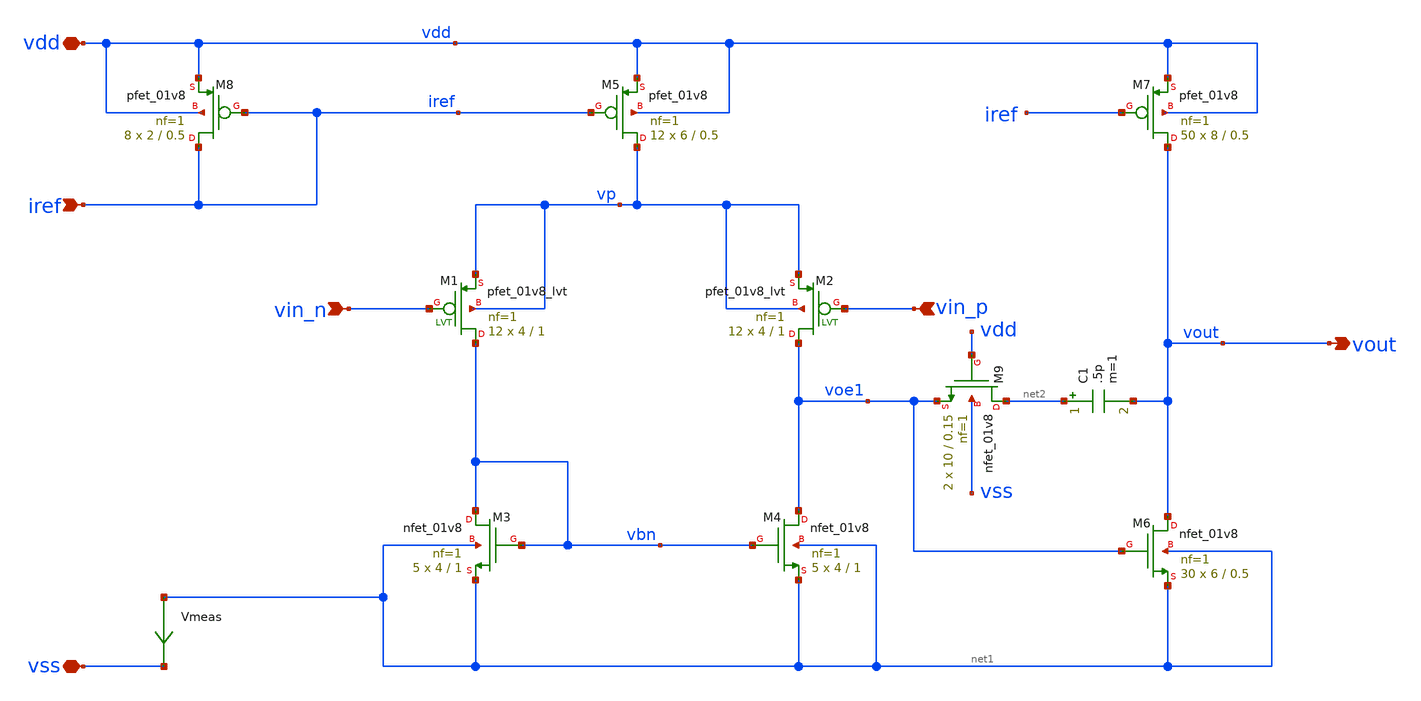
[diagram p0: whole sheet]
** sch_path: opamp/opamp.sch
**.subckt opamp vdd vss vin_n vin_p iref vout
*.iopin vdd
*.iopin vss
*.ipin vin_n
*.ipin vin_p
*.ipin iref
*.opin vout
XM3 vbn vbn net1 net1 sky130_fd_pr__nfet_01v8 L=1 W=4 nf=1 ad='W * 0.29' as='W * 0.29' pd='2 * (W + 0.29)'
+ ps='2 * (W + 0.29)' nrd='0.29 / W' nrs='0.29 / W' sa=0 sb=0 sd=0 mult=5 m=5
XM4 voe1 vbn net1 net1 sky130_fd_pr__nfet_01v8 L=1 W=4 nf=1 ad='W * 0.29' as='W * 0.29' pd='2 * (W + 0.29)'
+ ps='2 * (W + 0.29)' nrd='0.29 / W' nrs='0.29 / W' sa=0 sb=0 sd=0 mult=5 m=5
XM5 vp iref vdd vdd sky130_fd_pr__pfet_01v8 L=0.5 W=6 nf=1 ad='W * 0.29' as='W * 0.29' pd='2 * (W + 0.29)'
+ ps='2 * (W + 0.29)' nrd='0.29 / W' nrs='0.29 / W' sa=0 sb=0 sd=0 mult=12 m=12
XM7 vout iref vdd vdd sky130_fd_pr__pfet_01v8 L=0.5 W=8 nf=1 ad='W * 0.29' as='W * 0.29' pd='2 * (W + 0.29)'
+ ps='2 * (W + 0.29)' nrd='0.29 / W' nrs='0.29 / W' sa=0 sb=0 sd=0 mult=50 m=50
XM8 iref iref vdd vdd sky130_fd_pr__pfet_01v8 L=0.5 W=2 nf=1 ad='W * 0.29' as='W * 0.29' pd='2 * (W + 0.29)'
+ ps='2 * (W + 0.29)' nrd='0.29 / W' nrs='0.29 / W' sa=0 sb=0 sd=0 mult=8 m=8
XM9 net2 vdd voe1 vss sky130_fd_pr__nfet_01v8 L=0.15 W=10 nf=1 ad='W * 0.29' as='W * 0.29' pd='2 * (W + 0.29)'
+ ps='2 * (W + 0.29)' nrd='0.29 / W' nrs='0.29 / W' sa=0 sb=0 sd=0 mult=2 m=2
XM6 vout voe1 net1 net1 sky130_fd_pr__nfet_01v8 L=0.5 W=6 nf=1 ad='W * 0.29' as='W * 0.29' pd='2 * (W + 0.29)'
+ ps='2 * (W + 0.29)' nrd='0.29 / W' nrs='0.29 / W' sa=0 sb=0 sd=0 mult=30 m=30
XM1 vbn vin_n vp vp sky130_fd_pr__pfet_01v8_lvt L=1 W=4 nf=1 ad='int((nf+1)/2) * W/nf * 0.29' as='int((nf+2)/2) * W/nf * 0.29'
+ pd='2*int((nf+1)/2) * (W/nf + 0.29)' ps='2*int((nf+2)/2) * (W/nf + 0.29)' nrd='0.29 / W' nrs='0.29 / W'
+ sa=0 sb=0 sd=0 mult=12 m=12
XM2 voe1 vin_p vp vp sky130_fd_pr__pfet_01v8_lvt L=1 W=4 nf=1 ad='int((nf+1)/2) * W/nf * 0.29' as='int((nf+2)/2) * W/nf * 0.29'
+ pd='2*int((nf+1)/2) * (W/nf + 0.29)' ps='2*int((nf+2)/2) * (W/nf + 0.29)' nrd='0.29 / W' nrs='0.29 / W'
+ sa=0 sb=0 sd=0 mult=12 m=12
C1 net2 vout .5p m=1
Vmeas net1 vss 0
.save i(vmeas)
**.ends
.end
